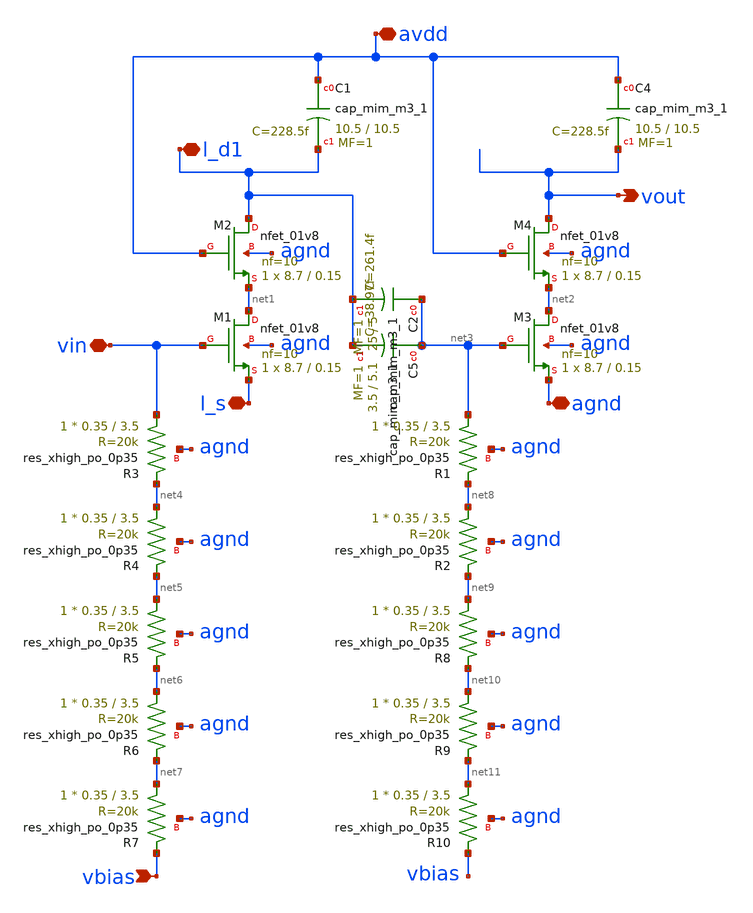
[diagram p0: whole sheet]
** sch_path: LNA/LNA.sch
**.subckt LNA avdd agnd vout vbias vin l_s l_d1
*.iopin avdd
*.iopin agnd
*.opin vout
*.ipin vbias
*.iopin vin
*.iopin l_s
*.iopin l_d1
XM1 net1 vin l_s agnd sky130_fd_pr__nfet_01v8 L=0.15 W=8.7 nf=10 ad='int((nf+1)/2) * W/nf * 0.29' as='int((nf+2)/2) * W/nf * 0.29'
+ pd='2*int((nf+1)/2) * (W/nf + 0.29)' ps='2*int((nf+2)/2) * (W/nf + 0.29)' nrd='0.29 / W' nrs='0.29 / W'
+ sa=0 sb=0 sd=0 mult=1 m=1
XC1 avdd l_d1 sky130_fd_pr__cap_mim_m3_1 W=10.5 L=10.5 MF=1 m=1
XM2 l_d1 avdd net1 agnd sky130_fd_pr__nfet_01v8 L=0.15 W=8.7 nf=10 ad='int((nf+1)/2) * W/nf * 0.29' as='int((nf+2)/2) * W/nf * 0.29'
+ pd='2*int((nf+1)/2) * (W/nf + 0.29)' ps='2*int((nf+2)/2) * (W/nf + 0.29)' nrd='0.29 / W' nrs='0.29 / W'
+ sa=0 sb=0 sd=0 mult=1 m=1
XM3 net2 net3 agnd agnd sky130_fd_pr__nfet_01v8 L=0.15 W=8.7 nf=10 ad='int((nf+1)/2) * W/nf * 0.29' as='int((nf+2)/2) * W/nf * 0.29'
+ pd='2*int((nf+1)/2) * (W/nf + 0.29)' ps='2*int((nf+2)/2) * (W/nf + 0.29)' nrd='0.29 / W' nrs='0.29 / W'
+ sa=0 sb=0 sd=0 mult=1 m=1
XM4 vout avdd net2 agnd sky130_fd_pr__nfet_01v8 L=0.15 W=8.7 nf=10 ad='int((nf+1)/2) * W/nf * 0.29' as='int((nf+2)/2) * W/nf * 0.29'
+ pd='2*int((nf+1)/2) * (W/nf + 0.29)' ps='2*int((nf+2)/2) * (W/nf + 0.29)' nrd='0.29 / W' nrs='0.29 / W'
+ sa=0 sb=0 sd=0 mult=1 m=1
XC4 avdd vout sky130_fd_pr__cap_mim_m3_1 W=10.5 L=10.5 MF=1 m=1
XC5 net3 l_d1 sky130_fd_pr__cap_mim_m3_1 W=3.5 L=5.1 MF=1 m=1
XR3 vin net4 agnd sky130_fd_pr__res_xhigh_po_0p35 L=3.5 mult=1 m=1
XR4 net4 net5 agnd sky130_fd_pr__res_xhigh_po_0p35 L=3.5 mult=1 m=1
XR5 net5 net6 agnd sky130_fd_pr__res_xhigh_po_0p35 L=3.5 mult=1 m=1
XR6 net6 net7 agnd sky130_fd_pr__res_xhigh_po_0p35 L=3.5 mult=1 m=1
XR7 net7 vbias agnd sky130_fd_pr__res_xhigh_po_0p35 L=3.5 mult=1 m=1
XR1 net3 net8 agnd sky130_fd_pr__res_xhigh_po_0p35 L=3.5 mult=1 m=1
XR2 net8 net9 agnd sky130_fd_pr__res_xhigh_po_0p35 L=3.5 mult=1 m=1
XR8 net9 net10 agnd sky130_fd_pr__res_xhigh_po_0p35 L=3.5 mult=1 m=1
XR9 net10 net11 agnd sky130_fd_pr__res_xhigh_po_0p35 L=3.5 mult=1 m=1
XR10 net11 vbias agnd sky130_fd_pr__res_xhigh_po_0p35 L=3.5 mult=1 m=1
XC2 net3 l_d1 sky130_fd_pr__cap_mim_m3_1 W=25 L=5 MF=1 m=1
**.ends
.end
